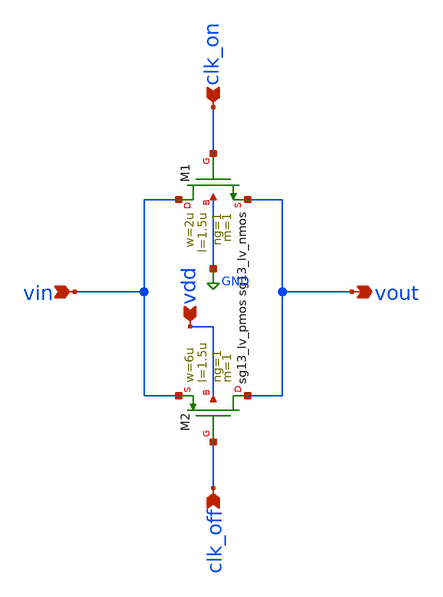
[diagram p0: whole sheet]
** sch_path: schematics/cmos_switch.sch
**.subckt cmos_switch vin clk_on clk_off vout vdd
*.ipin vin
*.ipin clk_on
*.ipin clk_off
*.opin vout
*.ipin vdd
XM1 vin clk_on vout GND sg13_lv_nmos w=2u l=1.5u ng=1 m=1 mm_ok=1
XM2 vout clk_off vin vdd sg13_lv_pmos w=6u l=1.5u ng=1 m=1 mm_ok=1
**.ends
.GLOBAL GND
.end
